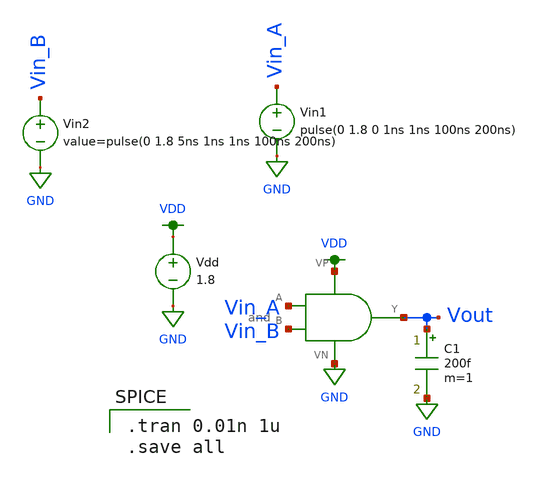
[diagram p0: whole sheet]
** sch_path: mp1/cmos_inverter/and_tran.sch
**.subckt and_tran
X1 Vin_A Vin_B Vout VDD GND and
Vdd VDD GND 1.8
C1 Vout GND 200f m=1
Vin2 Vin_B GND pulse(0 1.8 5ns 1ns 1ns 100ns 200ns)
Vin1 Vin_A GND pulse(0 1.8 0 1ns 1ns 100ns 200ns)
**** begin user architecture code

.tran 0.01n 1u
.save all


.option wnflag=1
.lib ~/skywater/skywater-pdk/libraries/sky130_fd_pr_ngspice/latest/models/sky130.lib.spice tt

**** end user architecture code
**.ends
.GLOBAL VDD
.GLOBAL GND
.end
